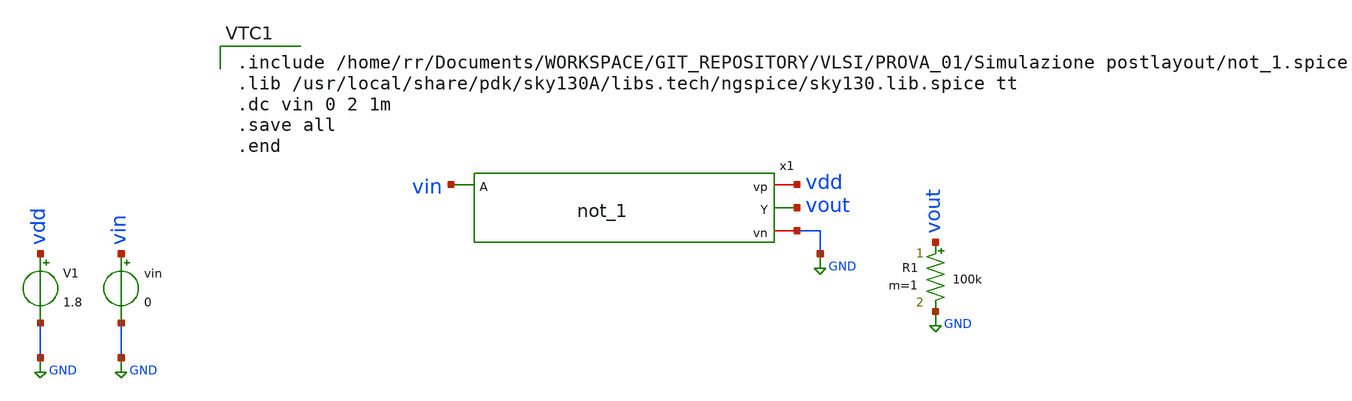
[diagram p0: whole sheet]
** sch_path: VLSI/PROVA_01/Simulazione postlayout/not_1_TB_postlayout.sch
**.subckt not_1_TB_postlayout
x1 vdd vin vout GND not_1
V1 vdd GND 1.8
vin vin GND 0
R1 vout GND 100k m=1
**** begin user architecture code

.include /home/rr/Documents/WORKSPACE/GIT_REPOSITORY/VLSI/PROVA_01/Simulazione postlayout/not_1.spice
.lib /usr/local/share/pdk/sky130A/libs.tech/ngspice/sky130.lib.spice tt
.dc vin 0 2 1m
.save all
.end

**** end user architecture code
**.ends
.GLOBAL GND
.end
